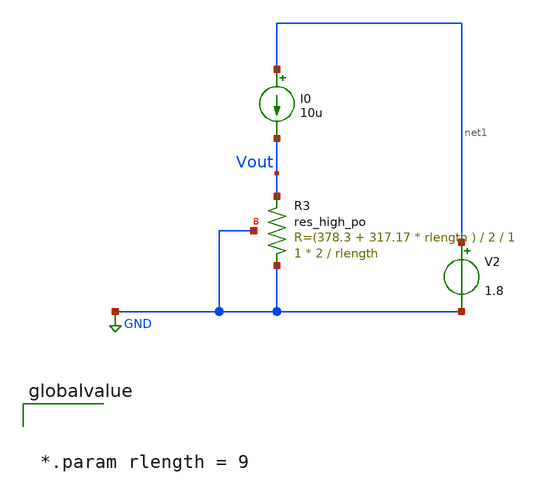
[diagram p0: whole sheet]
** sch_path: xschem/misc/testing/loop3.sch
**.subckt loop3
I0 net1 Vout 10u
V2 net1 GND 1.8
XR3 GND Vout GND sky130_fd_pr__res_high_po W=2 L=rlength mult=1 m=1
**** begin user architecture code

** opencircuitdesign pdks install
.lib $::SKYWATER_MODELS/sky130.lib.spice tt





*.param rlength = 9





.options savecurrents
.param rlength = 9

*** plot temperature coefficient
*Vdd VDD GND 3.3
*V_en en GND 3.3
*.dc temp -40 140 1
.control
*run
*dc temp -40 100 1
*plot Vout

save all
set appendwrite

compose length_vector values 1 50

let i = 0
while i < length(length_vector)
    reset
    echo 'assigning vectors'
    alterparam rlength = length_vector[i]
    echo 'Still assigning vectors'

    echo 'done assigning'
    dc temp -40 100 1
    plot Vout

    let i = i + 1
end


.endc



*** plot voltage coefficient
*Vdd VDD GND 3.3
*V_en en GND 3.3
*.dc Vdd 2 4 0.1
*.control
*run
*plot deriv(V(Vbgp))
*.endc

*** plot temperature coefficient
*Vdd VDD GND 3.3
*V_en en GND 3.3
*.dc temp -40 140 1
*.control
*run
*plot deriv(V(Vbgp))/1.202344
*.endc



*** enable pin
*Vdd VDD GND 3.3
*V_en en GND PULSE(0 3.3 0 200us 200us 600us 2000us 0)
*.tran 1u 2000us
*.control
*run
*plot V(en)
*plot -I(VDD)
*.endc


**** end user architecture code
**.ends
.GLOBAL GND
.end
